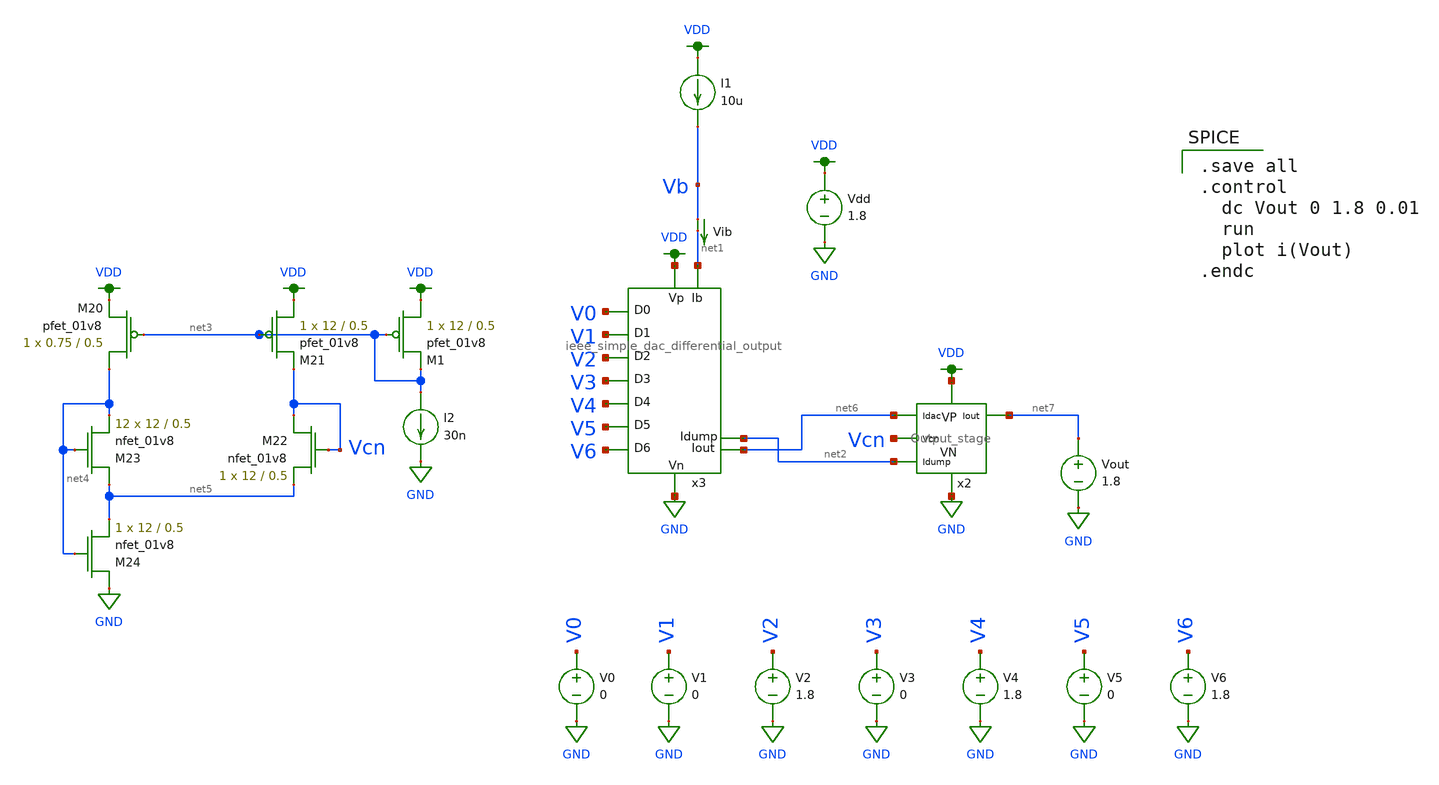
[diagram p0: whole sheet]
** sch_path: schematics/ieee DAC/ieee_DAC_mc_simulation_10.sch
**.subckt ieee_DAC_mc_simulation_10
Vdd VDD GND 1.8
V1 V1 GND 0
V2 V2 GND 1.8
V3 V3 GND 0
V4 V4 GND 1.8
V5 V5 GND 0
V6 V6 GND 1.8
V0 V0 GND 0
Vib Vb net1 0
.save i(vib)
I1 VDD Vb 10u
x2 VDD GND net7 Vcn net6 net2 Output_stage
x3 VDD net2 GND V1 V0 V2 V3 V4 V5 V6 net1 net6 ieee_simple_dac_differential_output
XM20 net4 net3 VDD VDD sky130_fd_pr__pfet_01v8 L=0.5 W=0.75 nf=1 ad='int((nf+1)/2) * W/nf * 0.29' as='int((nf+2)/2) * W/nf * 0.29'
+ pd='2*int((nf+1)/2) * (W/nf + 0.29)' ps='2*int((nf+2)/2) * (W/nf + 0.29)' nrd='0.29 / W' nrs='0.29 / W'
+ sa=0 sb=0 sd=0 mult=1 m=1
XM21 VDD net3 Vcn VDD sky130_fd_pr__pfet_01v8 L=0.5 W=12 nf=1 ad='int((nf+1)/2) * W/nf * 0.29' as='int((nf+2)/2) * W/nf * 0.29'
+ pd='2*int((nf+1)/2) * (W/nf + 0.29)' ps='2*int((nf+2)/2) * (W/nf + 0.29)' nrd='0.29 / W' nrs='0.29 / W'
+ sa=0 sb=0 sd=0 mult=1 m=1
XM22 Vcn Vcn net5 GND sky130_fd_pr__nfet_01v8 L=0.5 W=12 nf=1 ad='int((nf+1)/2) * W/nf * 0.29' as='int((nf+2)/2) * W/nf * 0.29'
+ pd='2*int((nf+1)/2) * (W/nf + 0.29)' ps='2*int((nf+2)/2) * (W/nf + 0.29)' nrd='0.29 / W' nrs='0.29 / W'
+ sa=0 sb=0 sd=0 mult=1 m=1
XM23 net5 net4 net4 GND sky130_fd_pr__nfet_01v8 L=0.5 W=12 nf=1 ad='int((nf+1)/2) * W/nf * 0.29' as='int((nf+2)/2) * W/nf * 0.29'
+ pd='2*int((nf+1)/2) * (W/nf + 0.29)' ps='2*int((nf+2)/2) * (W/nf + 0.29)' nrd='0.29 / W' nrs='0.29 / W'
+ sa=0 sb=0 sd=0 mult=12 m=12
XM24 GND net4 net5 GND sky130_fd_pr__nfet_01v8 L=0.5 W=12 nf=1 ad='int((nf+1)/2) * W/nf * 0.29' as='int((nf+2)/2) * W/nf * 0.29'
+ pd='2*int((nf+1)/2) * (W/nf + 0.29)' ps='2*int((nf+2)/2) * (W/nf + 0.29)' nrd='0.29 / W' nrs='0.29 / W'
+ sa=0 sb=0 sd=0 mult=1 m=1
I2 net3 GND 30n
Vout net7 GND 1.8
XM1 VDD net3 net3 VDD sky130_fd_pr__pfet_01v8 L=0.5 W=12 nf=1 ad='int((nf+1)/2) * W/nf * 0.29' as='int((nf+2)/2) * W/nf * 0.29'
+ pd='2*int((nf+1)/2) * (W/nf + 0.29)' ps='2*int((nf+2)/2) * (W/nf + 0.29)' nrd='0.29 / W' nrs='0.29 / W'
+ sa=0 sb=0 sd=0 mult=1 m=1
**** begin user architecture code

.option wnflag=1
.param MC_SWITCH=0.0
.lib ~/skywater/skywater-pdk/libraries/sky130_fd_pr_ngspice/latest/models/sky130.lib.spice tt


.save all
.control
  dc Vout 0 1.8 0.01
  run
  plot i(Vout)
.endc

**** end user architecture code
**.ends
.GLOBAL VDD
.GLOBAL GND
.end
